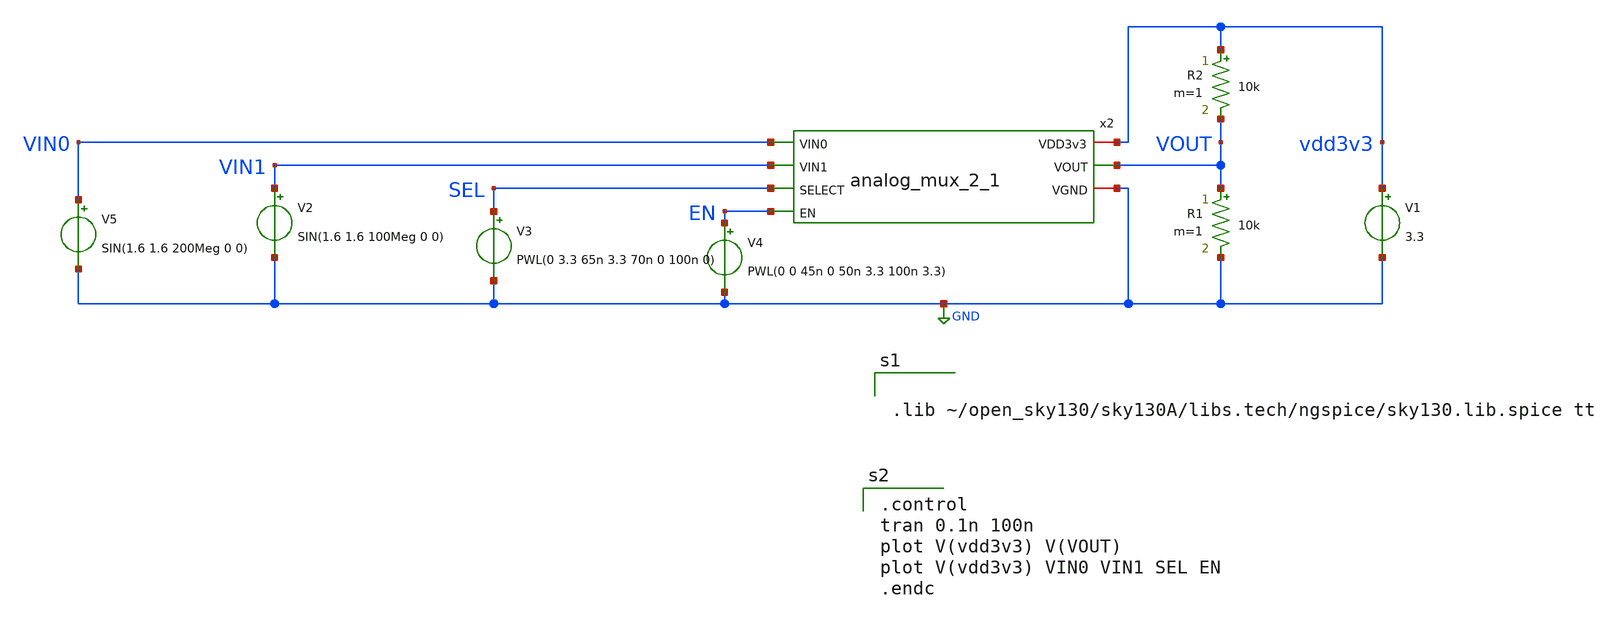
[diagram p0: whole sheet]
** sch_path: xschem/analog_mux/analogue_mux_tb.sch
**.subckt analogue_mux_tb
V1 vdd3v3 GND 3.3
V2 VIN1 GND SIN(1.6 1.6 100Meg 0 0)
V3 SEL GND PWL(0 3.3 65n 3.3 70n 0 100n 0)
V4 EN GND PWL(0 0 45n 0 50n 3.3 100n 3.3)
R1 VOUT GND 10k m=1
R2 vdd3v3 VOUT 10k m=1
x2 vdd3v3 VIN0 VOUT VIN1 GND SEL EN analog_mux_2_1
V5 VIN0 GND SIN(1.6 1.6 200Meg 0 0)
**** begin user architecture code


.lib ~/open_sky130/sky130A/libs.tech/ngspice/sky130.lib.spice tt


.control
tran 0.1n 100n
plot V(vdd3v3) V(VOUT)
plot V(vdd3v3) VIN0 VIN1 SEL EN
.endc

**** end user architecture code
**.ends

* expanding   symbol:  analog_mux_2_1.sym # of pins=7
** sym_path: xschem/analog_mux_2_1.sym
** sch_path: xschem/analog_mux_2_1.sch
.subckt analog_mux_2_1 VDD3v3 VIN0 VOUT VIN1 VGND SELECT EN
*.iopin VGND
*.ipin VIN0
*.opin VOUT
*.iopin VDD3v3
*.ipin VIN1
*.ipin EN
*.ipin SELECT
x1 VIN0 VGND VDD3v3 !EN0 EN0 VOUT analogue_switch
x2 VIN1 VGND VDD3v3 !EN1 EN1 VOUT analogue_switch
XM3 !EN1 SELECT VDD3v3 VDD3v3 sky130_fd_pr__pfet_g5v0d10v5 L=0.5 W=0.75 nf=1 ad='int((nf+1)/2) * W/nf * 0.29'
+ as='int((nf+2)/2) * W/nf * 0.29' pd='2*int((nf+1)/2) * (W/nf + 0.29)' ps='2*int((nf+2)/2) * (W/nf + 0.29)'
+ nrd='0.29 / W' nrs='0.29 / W' sa=0 sb=0 sd=0 mult=1 m=1
XM4 !EN1 EN VDD3v3 VDD3v3 sky130_fd_pr__pfet_g5v0d10v5 L=0.5 W=0.75 nf=1 ad='int((nf+1)/2) * W/nf * 0.29'
+ as='int((nf+2)/2) * W/nf * 0.29' pd='2*int((nf+1)/2) * (W/nf + 0.29)' ps='2*int((nf+2)/2) * (W/nf + 0.29)'
+ nrd='0.29 / W' nrs='0.29 / W' sa=0 sb=0 sd=0 mult=1 m=1
XM2 net1 SELECT VGND VGND sky130_fd_pr__nfet_03v3_nvt L=0.5 W=0.7 nf=1 ad='int((nf+1)/2) * W/nf * 0.29'
+ as='int((nf+2)/2) * W/nf * 0.29' pd='2*int((nf+1)/2) * (W/nf + 0.29)' ps='2*int((nf+2)/2) * (W/nf + 0.29)'
+ nrd='0.29 / W' nrs='0.29 / W' sa=0 sb=0 sd=0 mult=1 m=1
XM5 !EN1 EN net1 VGND sky130_fd_pr__nfet_03v3_nvt L=0.5 W=0.7 nf=1 ad='int((nf+1)/2) * W/nf * 0.29' as='int((nf+2)/2) * W/nf * 0.29'
+ pd='2*int((nf+1)/2) * (W/nf + 0.29)' ps='2*int((nf+2)/2) * (W/nf + 0.29)' nrd='0.29 / W' nrs='0.29 / W'
+ sa=0 sb=0 sd=0 mult=1 m=1
XM1 EN1 !EN1 VDD3v3 VDD3v3 sky130_fd_pr__pfet_g5v0d10v5 L=0.5 W=0.75 nf=1 ad='int((nf+1)/2) * W/nf * 0.29'
+ as='int((nf+2)/2) * W/nf * 0.29' pd='2*int((nf+1)/2) * (W/nf + 0.29)' ps='2*int((nf+2)/2) * (W/nf + 0.29)'
+ nrd='0.29 / W' nrs='0.29 / W' sa=0 sb=0 sd=0 mult=1 m=1
XM6 EN1 !EN1 VGND VGND sky130_fd_pr__nfet_03v3_nvt L=0.5 W=0.7 nf=1 ad='int((nf+1)/2) * W/nf * 0.29'
+ as='int((nf+2)/2) * W/nf * 0.29' pd='2*int((nf+1)/2) * (W/nf + 0.29)' ps='2*int((nf+2)/2) * (W/nf + 0.29)'
+ nrd='0.29 / W' nrs='0.29 / W' sa=0 sb=0 sd=0 mult=1 m=1
XM7 !SELECT SELECT VDD3v3 VDD3v3 sky130_fd_pr__pfet_g5v0d10v5 L=0.5 W=0.75 nf=1 ad='int((nf+1)/2) * W/nf * 0.29'
+ as='int((nf+2)/2) * W/nf * 0.29' pd='2*int((nf+1)/2) * (W/nf + 0.29)' ps='2*int((nf+2)/2) * (W/nf + 0.29)'
+ nrd='0.29 / W' nrs='0.29 / W' sa=0 sb=0 sd=0 mult=1 m=1
XM8 !SELECT SELECT VGND VGND sky130_fd_pr__nfet_03v3_nvt L=0.5 W=0.7 nf=1 ad='int((nf+1)/2) * W/nf * 0.29'
+ as='int((nf+2)/2) * W/nf * 0.29' pd='2*int((nf+1)/2) * (W/nf + 0.29)' ps='2*int((nf+2)/2) * (W/nf + 0.29)'
+ nrd='0.29 / W' nrs='0.29 / W' sa=0 sb=0 sd=0 mult=1 m=1
XM9 !EN0 EN VDD3v3 VDD3v3 sky130_fd_pr__pfet_g5v0d10v5 L=0.5 W=0.75 nf=1 ad='int((nf+1)/2) * W/nf * 0.29'
+ as='int((nf+2)/2) * W/nf * 0.29' pd='2*int((nf+1)/2) * (W/nf + 0.29)' ps='2*int((nf+2)/2) * (W/nf + 0.29)'
+ nrd='0.29 / W' nrs='0.29 / W' sa=0 sb=0 sd=0 mult=1 m=1
XM10 net2 !SELECT VGND VGND sky130_fd_pr__nfet_03v3_nvt L=0.5 W=0.7 nf=1 ad='int((nf+1)/2) * W/nf * 0.29'
+ as='int((nf+2)/2) * W/nf * 0.29' pd='2*int((nf+1)/2) * (W/nf + 0.29)' ps='2*int((nf+2)/2) * (W/nf + 0.29)'
+ nrd='0.29 / W' nrs='0.29 / W' sa=0 sb=0 sd=0 mult=1 m=1
XM11 !EN0 EN net2 VGND sky130_fd_pr__nfet_03v3_nvt L=0.5 W=0.7 nf=1 ad='int((nf+1)/2) * W/nf * 0.29'
+ as='int((nf+2)/2) * W/nf * 0.29' pd='2*int((nf+1)/2) * (W/nf + 0.29)' ps='2*int((nf+2)/2) * (W/nf + 0.29)'
+ nrd='0.29 / W' nrs='0.29 / W' sa=0 sb=0 sd=0 mult=1 m=1
XM12 EN0 !EN0 VDD3v3 VDD3v3 sky130_fd_pr__pfet_g5v0d10v5 L=0.5 W=0.75 nf=1 ad='int((nf+1)/2) * W/nf * 0.29'
+ as='int((nf+2)/2) * W/nf * 0.29' pd='2*int((nf+1)/2) * (W/nf + 0.29)' ps='2*int((nf+2)/2) * (W/nf + 0.29)'
+ nrd='0.29 / W' nrs='0.29 / W' sa=0 sb=0 sd=0 mult=1 m=1
XM13 EN0 !EN0 VGND VGND sky130_fd_pr__nfet_03v3_nvt L=0.5 W=0.7 nf=1 ad='int((nf+1)/2) * W/nf * 0.29'
+ as='int((nf+2)/2) * W/nf * 0.29' pd='2*int((nf+1)/2) * (W/nf + 0.29)' ps='2*int((nf+2)/2) * (W/nf + 0.29)'
+ nrd='0.29 / W' nrs='0.29 / W' sa=0 sb=0 sd=0 mult=1 m=1
XM14 !EN0 !SELECT VDD3v3 VDD3v3 sky130_fd_pr__pfet_g5v0d10v5 L=0.5 W=0.75 nf=1 ad='int((nf+1)/2) * W/nf * 0.29'
+ as='int((nf+2)/2) * W/nf * 0.29' pd='2*int((nf+1)/2) * (W/nf + 0.29)' ps='2*int((nf+2)/2) * (W/nf + 0.29)'
+ nrd='0.29 / W' nrs='0.29 / W' sa=0 sb=0 sd=0 mult=1 m=1
.ends


* expanding   symbol:  analogue_switch.sym # of pins=6
** sym_path: xschem/analogue_switch.sym
** sch_path: xschem/analogue_switch.sch
.subckt analogue_switch VIN VGND VDD3v3 !EN EN VOUT
*.iopin VGND
*.iopin VDD3v3
*.ipin EN
*.ipin VIN
*.ipin !EN
*.opin VOUT
XM2 VOUT !EN VIN VDD3v3 sky130_fd_pr__pfet_g5v0d10v5 L=0.5 W=1 nf=1 ad='int((nf+1)/2) * W/nf * 0.29'
+ as='int((nf+2)/2) * W/nf * 0.29' pd='2*int((nf+1)/2) * (W/nf + 0.29)' ps='2*int((nf+2)/2) * (W/nf + 0.29)'
+ nrd='0.29 / W' nrs='0.29 / W' sa=0 sb=0 sd=0 mult=1 m=1
XM1 VIN EN VOUT VGND sky130_fd_pr__nfet_03v3_nvt L=0.5 W=1 nf=1 ad='int((nf+1)/2) * W/nf * 0.29' as='int((nf+2)/2) * W/nf * 0.29'
+ pd='2*int((nf+1)/2) * (W/nf + 0.29)' ps='2*int((nf+2)/2) * (W/nf + 0.29)' nrd='0.29 / W' nrs='0.29 / W'
+ sa=0 sb=0 sd=0 mult=1 m=1
.ends

.GLOBAL GND
.end
